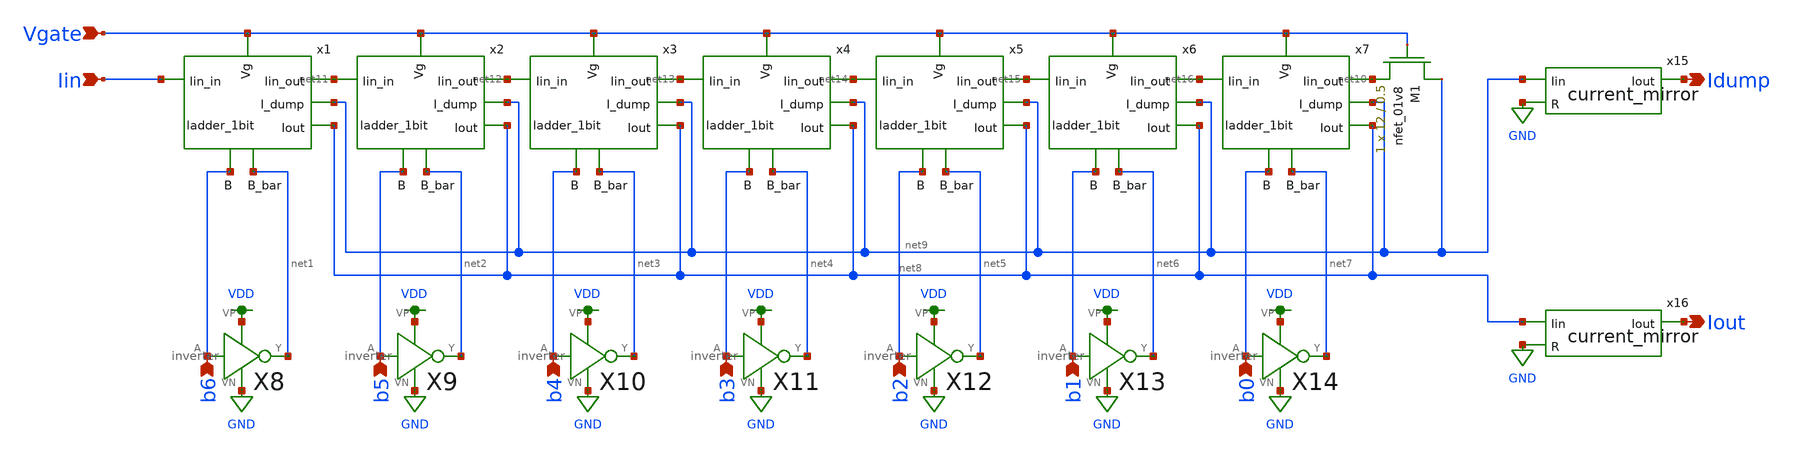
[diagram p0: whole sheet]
** sch_path: ladder_7bit.sch
**.subckt ladder_7bit Idump Vgate Iin b6 b5 b4 b3 b2 b1 b0 Iout
*.opin Idump
*.ipin Vgate
*.ipin Iin
*.ipin b6
*.ipin b5
*.ipin b4
*.ipin b3
*.ipin b2
*.ipin b1
*.ipin b0
*.opin Iout
XM1 net9 Vgate net10 GND sky130_fd_pr__nfet_01v8 L=0.5 W=12 nf=1 ad='int((nf+1)/2) * W/nf * 0.29' as='int((nf+2)/2) * W/nf * 0.29'
+ pd='2*int((nf+1)/2) * (W/nf + 0.29)' ps='2*int((nf+2)/2) * (W/nf + 0.29)' nrd='0.29 / W' nrs='0.29 / W'
+ sa=0 sb=0 sd=0 mult=1 m=1
x1 Iin net11 Vgate net9 net8 net1 b6 ladder_1bit
X8 b6 net1 VDD GND inverter
X9 b5 net2 VDD GND inverter
X10 b4 net3 VDD GND inverter
X11 b3 net4 VDD GND inverter
X12 b2 net5 VDD GND inverter
X13 b1 net6 VDD GND inverter
X14 b0 net7 VDD GND inverter
x2 net11 net12 Vgate net9 net8 net2 b5 ladder_1bit
x3 net12 net13 Vgate net9 net8 net3 b4 ladder_1bit
x4 net13 net14 Vgate net9 net8 net4 b3 ladder_1bit
x5 net14 net15 Vgate net9 net8 net5 b2 ladder_1bit
x6 net15 net16 Vgate net9 net8 net6 b1 ladder_1bit
x7 net16 net10 Vgate net9 net8 net7 b0 ladder_1bit
x15 Idump net9 GND current_mirror
x16 Iout net8 GND current_mirror
**.ends
.GLOBAL VDD
.GLOBAL GND
.end
